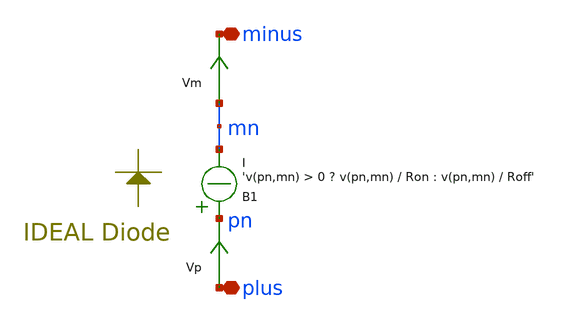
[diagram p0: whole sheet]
** sch_path: xschem-src/xschem_library/ngspice/diode_ngspice.sch
* Copyright (C) 1998-2026 Stefan Frederik Schippers
* This program is free software; you can redistribute it and/or modify
* it under the terms of the GNU General Public License as published by
* the Free Software Foundation; either version 2 of the License, or
* (at your option) any later version.
* This program is distributed in the hope that it will be useful,
* but WITHOUT ANY WARRANTY; without even the implied warranty of
* MERCHANTABILITY or FITNESS FOR A PARTICULAR PURPOSE.  See the
* GNU General Public License for more details.
* You should have received a copy of the GNU General Public License
* along with this program; if not, write to the Free Software
**.subckt diode_ngspice plus minus
*.iopin plus
*.iopin minus
Vm mn minus 0
.save i(vm)
Vp plus pn 0
.save i(vp)
B1 pn mn I = 'v(pn,mn) > 0 ? v(pn,mn) / Ron : v(pn,mn) / Roff'
**.ends
.end
